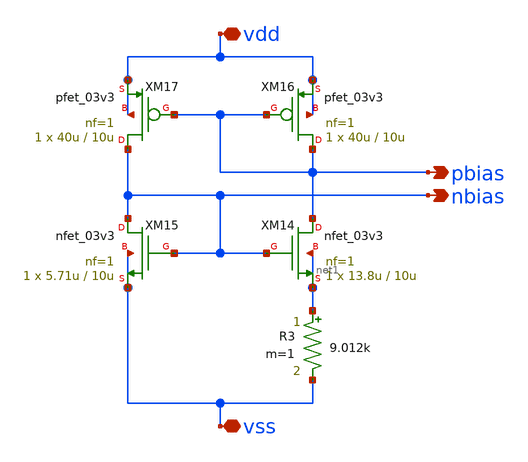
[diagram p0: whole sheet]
** sch_path: design/analog/beta multiplier/beta_multiplier.sch
**.subckt beta_multiplier vdd vss pbias nbias
*.iopin vdd
*.iopin vss
*.opin pbias
*.opin nbias
XM14 pbias nbias net1 net1 nfet_03v3 L=10u W=13.8u nf=1 ad='int((nf+1)/2) * W/nf * 0.18u' as='int((nf+2)/2) * W/nf * 0.18u'
+ pd='2*int((nf+1)/2) * (W/nf + 0.18u)' ps='2*int((nf+2)/2) * (W/nf + 0.18u)' nrd='0.18u / W' nrs='0.18u / W'
+ sa=0 sb=0 sd=0 m=1
XM15 nbias nbias vss vss nfet_03v3 L=10u W=5.71u nf=1 ad='int((nf+1)/2) * W/nf * 0.18u' as='int((nf+2)/2) * W/nf * 0.18u'
+ pd='2*int((nf+1)/2) * (W/nf + 0.18u)' ps='2*int((nf+2)/2) * (W/nf + 0.18u)' nrd='0.18u / W' nrs='0.18u / W'
+ sa=0 sb=0 sd=0 m=1
XM16 pbias pbias vdd vdd pfet_03v3 L=10u W=40u nf=1 ad='int((nf+1)/2) * W/nf * 0.18u' as='int((nf+2)/2) * W/nf * 0.18u'
+ pd='2*int((nf+1)/2) * (W/nf + 0.18u)' ps='2*int((nf+2)/2) * (W/nf + 0.18u)' nrd='0.18u / W' nrs='0.18u / W'
+ sa=0 sb=0 sd=0 m=1
XM17 nbias pbias vdd vdd pfet_03v3 L=10u W=40u nf=1 ad='int((nf+1)/2) * W/nf * 0.18u' as='int((nf+2)/2) * W/nf * 0.18u'
+ pd='2*int((nf+1)/2) * (W/nf + 0.18u)' ps='2*int((nf+2)/2) * (W/nf + 0.18u)' nrd='0.18u / W' nrs='0.18u / W'
+ sa=0 sb=0 sd=0 m=1
R3 net1 vss 9.012k m=1
**.ends
.end
